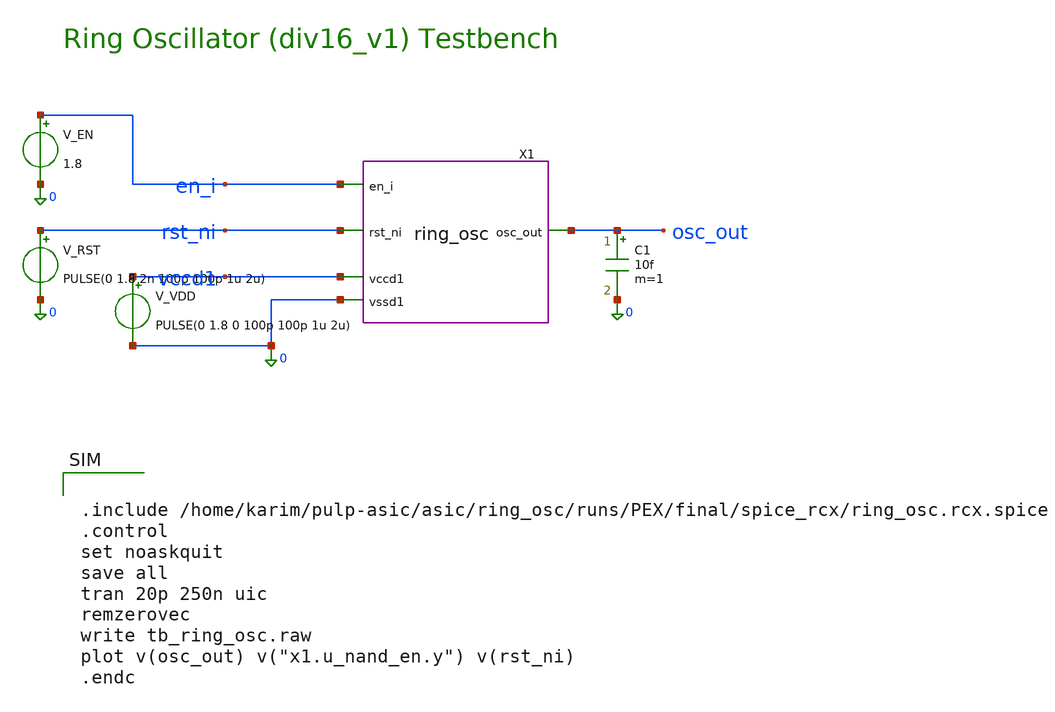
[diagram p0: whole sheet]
** sch_path: asic/ring_osc/tb_ring_osc.sch
**.subckt tb_ring_osc
X1 en_i osc_out rst_ni vccd1 0 ring_osc
V_VDD vccd1 0 PULSE(0 1.8 0 100p 100p 1u 2u)
V_RST rst_ni 0 PULSE(0 1.8 2n 100p 100p 1u 2u)
V_EN en_i 0 1.8
C1 osc_out 0 10f m=1
**** begin user architecture code

.lib $::SKYWATER_MODELS/sky130.lib.spice tt



.include /home/karim/pulp-asic/asic/ring_osc/runs/PEX/final/spice_rcx/ring_osc.rcx.spice
.control
set noaskquit
save all
tran 20p 250n uic
remzerovec
write tb_ring_osc.raw
plot v(osc_out) v("x1.u_nand_en.y") v(rst_ni)
.endc


**** end user architecture code
**.ends
.end
